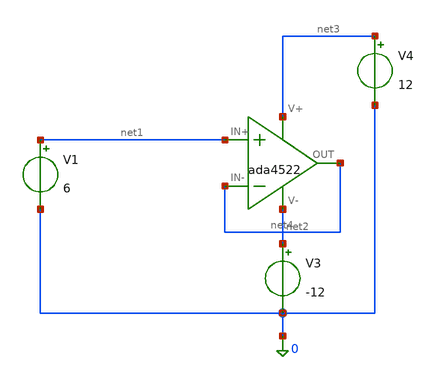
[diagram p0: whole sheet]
** sch_path: sim/xschem/ADA4522_TEST.sch
**.subckt ADA4522_TEST
x1 net1 net4 net3 net2 net4 ada4522
V1 net1 0 6
V3 net2 0 -12
V4 net3 0 12
**** begin user architecture code

.op

**** end user architecture code
**.ends

* expanding   symbol:  /foss/designs/sim/xschem/symbols/ada4522.sym # of pins=5
** sym_path: sim/xschem/symbols/ada4522.sym
.include /foss/designs/sim/models/ada4522.cir
.end
